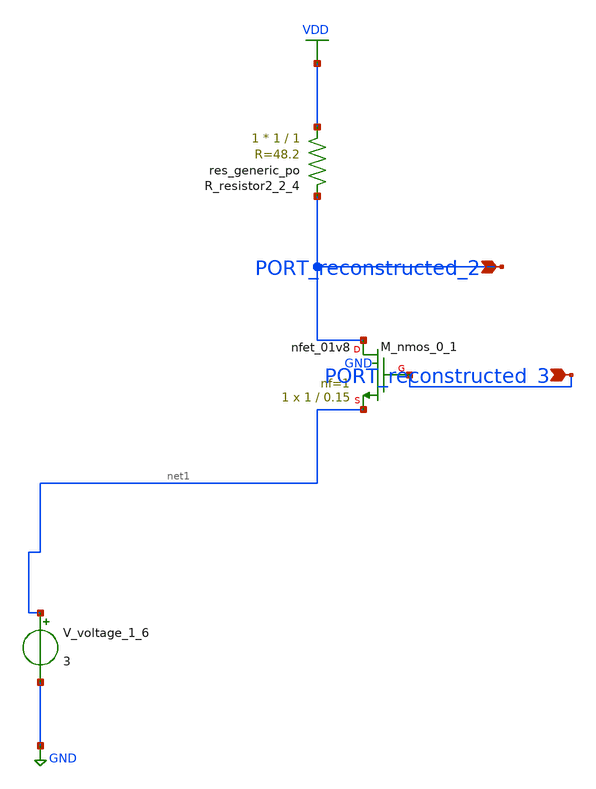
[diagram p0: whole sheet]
** sch_path: schematics/AMSNet/112.sch
**.subckt 112 PORT_reconstructed_3 PORT_reconstructed_2
*.ipin PORT_reconstructed_3
*.ipin PORT_reconstructed_2
XM_nmos_0_1 PORT_reconstructed_2 PORT_reconstructed_3 net1 GND sky130_fd_pr__nfet_01v8 L=0.15 W=1 nf=1
+ ad='int((1 + 1)/2) * 1 / 1 * 0.29' as='int((1 + 2)/2) * 1 / 1 * 0.29' pd='2*int((1 + 1)/2) * (1 / 1 + 0.29)'
+ ps='2*int((1 + 2)/2) * (1 / 1 + 0.29)' nrd='0.29 / 1 ' nrs='0.29 / 1 ' sa=0 sb=0 sd=0 mult=1 m=1
XR_resistor2_2_4 VDD PORT_reconstructed_2 sky130_fd_pr__res_generic_po W=1 L=1 m=1
V_voltage_1_6 net1 GND 3
**.ends
.GLOBAL GND
.GLOBAL VDD
.end
